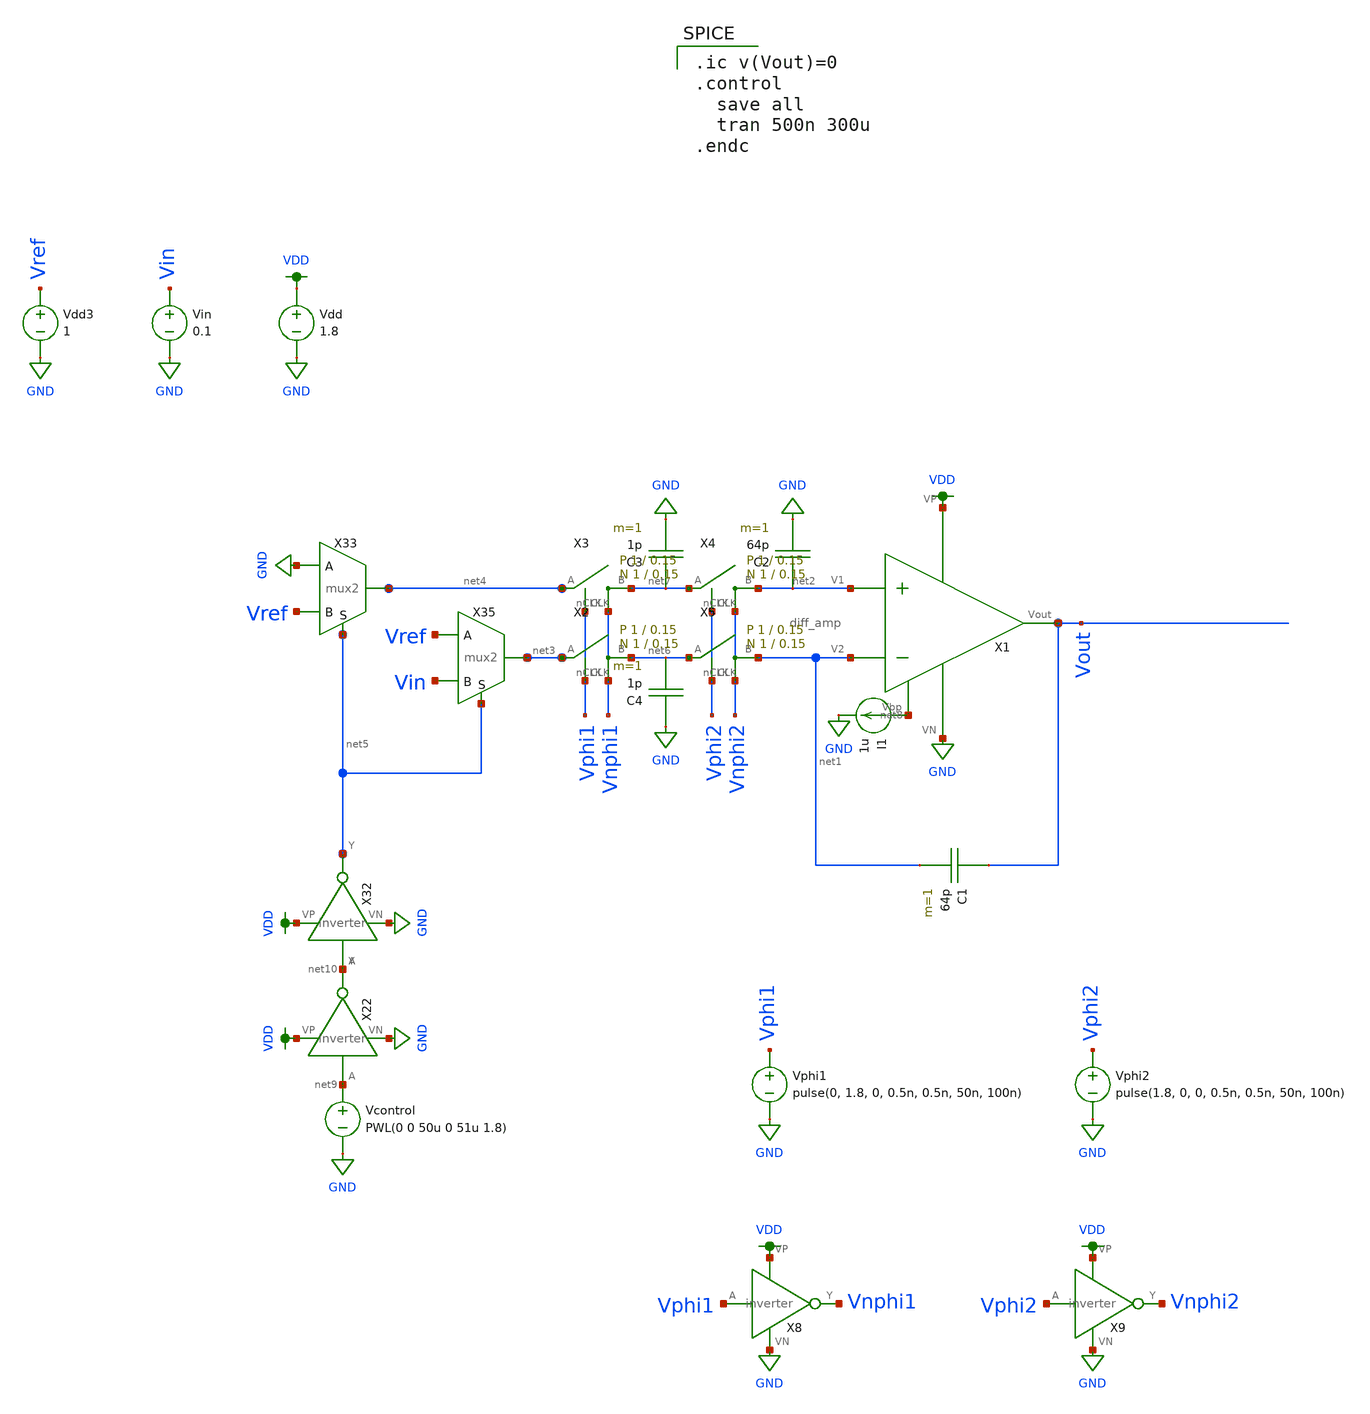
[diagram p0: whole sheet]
** sch_path: schematic/integrator.sch
**.subckt integrator
Vdd VDD GND 1.8
Vin Vin GND 0.1
C1 Vout net1 64p m=1
X1 VDD net8 Vout net2 net1 GND diff_amp
C2 net2 GND 64p m=1
I1 net8 GND 1u
Vdd3 Vref GND 1
Vcontrol net9 GND PWL(0 0 50u 0 51u 1.8)
X22 net9 net10 VDD GND inverter
X32 net10 net5 VDD GND inverter
X33 net4 GND Vref net5 mux2
X35 net3 Vref Vin net5 mux2
C3 net7 GND 1p m=1
C4 GND net6 1p m=1
Vphi1 Vphi1 GND pulse(0, 1.8, 0, 0.5n, 0.5n, 50n, 100n)
X8 Vphi1 Vnphi1 VDD GND inverter
Vphi2 Vphi2 GND pulse(1.8, 0, 0, 0.5n, 0.5n, 50n, 100n)
X9 Vphi2 Vnphi2 VDD GND inverter
X2 net6 net3 Vphi1 Vnphi1 switch Wp=1 Lp=0.15 WW=1 LL=0.15
X3 net7 net4 Vphi1 Vnphi1 switch Wp=1 Lp=0.15 WW=1 LL=0.15
X4 net2 net7 Vphi2 Vnphi2 switch Wp=1 Lp=0.15 WW=1 LL=0.15
X5 net1 net6 Vphi2 Vnphi2 switch Wp=1 Lp=0.15 WW=1 LL=0.15
**** begin user architecture code

.ic v(Vout)=0
.control
  save all
  tran 500n 300u
.endc


.option wnflag=1
.param MC_SWITCH=0.0
.lib ~/skywater/skywater-pdk/libraries/sky130_fd_pr_ngspice/latest/models/sky130.lib.spice tt

**** end user architecture code
**.ends
.GLOBAL GND
.GLOBAL VDD
.end
